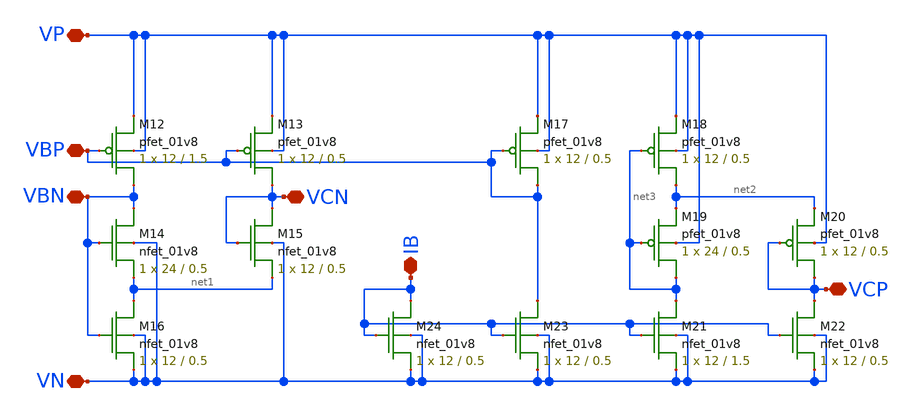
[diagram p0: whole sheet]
** sch_path: mp3/schematics/bias_generator.sch
**.subckt bias_generator VP VN IB VBP VCN VCP VBN
*.iopin VP
*.iopin VN
*.iopin IB
*.iopin VBP
*.iopin VCN
*.iopin VCP
*.iopin VBN
XM12 VBN VBP VP VP sky130_fd_pr__pfet_01v8 L=1.5 W=12 nf=1 ad='int((nf+1)/2) * W/nf * 0.29' as='int((nf+2)/2) * W/nf * 0.29'
+ pd='2*int((nf+1)/2) * (W/nf + 0.29)' ps='2*int((nf+2)/2) * (W/nf + 0.29)' nrd='0.29 / W' nrs='0.29 / W'
+ sa=0 sb=0 sd=0 mult=1 m=1
XM13 VCN VBP VP VP sky130_fd_pr__pfet_01v8 L=0.5 W=12 nf=1 ad='int((nf+1)/2) * W/nf * 0.29' as='int((nf+2)/2) * W/nf * 0.29'
+ pd='2*int((nf+1)/2) * (W/nf + 0.29)' ps='2*int((nf+2)/2) * (W/nf + 0.29)' nrd='0.29 / W' nrs='0.29 / W'
+ sa=0 sb=0 sd=0 mult=1 m=1
XM19 net3 net3 net2 VP sky130_fd_pr__pfet_01v8 L=0.5 W=24 nf=1 ad='int((nf+1)/2) * W/nf * 0.29' as='int((nf+2)/2) * W/nf * 0.29'
+ pd='2*int((nf+1)/2) * (W/nf + 0.29)' ps='2*int((nf+2)/2) * (W/nf + 0.29)' nrd='0.29 / W' nrs='0.29 / W'
+ sa=0 sb=0 sd=0 mult=1 m=1
XM20 VCP VCP net2 VP sky130_fd_pr__pfet_01v8 L=0.5 W=12 nf=1 ad='int((nf+1)/2) * W/nf * 0.29' as='int((nf+2)/2) * W/nf * 0.29'
+ pd='2*int((nf+1)/2) * (W/nf + 0.29)' ps='2*int((nf+2)/2) * (W/nf + 0.29)' nrd='0.29 / W' nrs='0.29 / W'
+ sa=0 sb=0 sd=0 mult=1 m=1
XM18 net2 net3 VP VP sky130_fd_pr__pfet_01v8 L=0.5 W=12 nf=1 ad='int((nf+1)/2) * W/nf * 0.29' as='int((nf+2)/2) * W/nf * 0.29'
+ pd='2*int((nf+1)/2) * (W/nf + 0.29)' ps='2*int((nf+2)/2) * (W/nf + 0.29)' nrd='0.29 / W' nrs='0.29 / W'
+ sa=0 sb=0 sd=0 mult=1 m=1
XM22 VCP IB VN VN sky130_fd_pr__nfet_01v8 L=0.5 W=12 nf=1 ad='int((nf+1)/2) * W/nf * 0.29' as='int((nf+2)/2) * W/nf * 0.29'
+ pd='2*int((nf+1)/2) * (W/nf + 0.29)' ps='2*int((nf+2)/2) * (W/nf + 0.29)' nrd='0.29 / W' nrs='0.29 / W'
+ sa=0 sb=0 sd=0 mult=1 m=1
XM21 net3 IB VN VN sky130_fd_pr__nfet_01v8 L=1.5 W=12 nf=1 ad='int((nf+1)/2) * W/nf * 0.29' as='int((nf+2)/2) * W/nf * 0.29'
+ pd='2*int((nf+1)/2) * (W/nf + 0.29)' ps='2*int((nf+2)/2) * (W/nf + 0.29)' nrd='0.29 / W' nrs='0.29 / W'
+ sa=0 sb=0 sd=0 mult=1 m=1
XM23 VBP IB VN VN sky130_fd_pr__nfet_01v8 L=0.5 W=12 nf=1 ad='int((nf+1)/2) * W/nf * 0.29' as='int((nf+2)/2) * W/nf * 0.29'
+ pd='2*int((nf+1)/2) * (W/nf + 0.29)' ps='2*int((nf+2)/2) * (W/nf + 0.29)' nrd='0.29 / W' nrs='0.29 / W'
+ sa=0 sb=0 sd=0 mult=1 m=1
XM24 IB IB VN VN sky130_fd_pr__nfet_01v8 L=0.5 W=12 nf=1 ad='int((nf+1)/2) * W/nf * 0.29' as='int((nf+2)/2) * W/nf * 0.29'
+ pd='2*int((nf+1)/2) * (W/nf + 0.29)' ps='2*int((nf+2)/2) * (W/nf + 0.29)' nrd='0.29 / W' nrs='0.29 / W'
+ sa=0 sb=0 sd=0 mult=1 m=1
XM15 VCN VCN net1 VN sky130_fd_pr__nfet_01v8 L=0.5 W=12 nf=1 ad='int((nf+1)/2) * W/nf * 0.29' as='int((nf+2)/2) * W/nf * 0.29'
+ pd='2*int((nf+1)/2) * (W/nf + 0.29)' ps='2*int((nf+2)/2) * (W/nf + 0.29)' nrd='0.29 / W' nrs='0.29 / W'
+ sa=0 sb=0 sd=0 mult=1 m=1
XM14 VBN VBN net1 VN sky130_fd_pr__nfet_01v8 L=0.5 W=24 nf=1 ad='int((nf+1)/2) * W/nf * 0.29' as='int((nf+2)/2) * W/nf * 0.29'
+ pd='2*int((nf+1)/2) * (W/nf + 0.29)' ps='2*int((nf+2)/2) * (W/nf + 0.29)' nrd='0.29 / W' nrs='0.29 / W'
+ sa=0 sb=0 sd=0 mult=1 m=1
XM16 net1 VBN VN VN sky130_fd_pr__nfet_01v8 L=0.5 W=12 nf=1 ad='int((nf+1)/2) * W/nf * 0.29' as='int((nf+2)/2) * W/nf * 0.29'
+ pd='2*int((nf+1)/2) * (W/nf + 0.29)' ps='2*int((nf+2)/2) * (W/nf + 0.29)' nrd='0.29 / W' nrs='0.29 / W'
+ sa=0 sb=0 sd=0 mult=1 m=1
XM17 VBP VBP VP VP sky130_fd_pr__pfet_01v8 L=0.5 W=12 nf=1 ad='int((nf+1)/2) * W/nf * 0.29' as='int((nf+2)/2) * W/nf * 0.29'
+ pd='2*int((nf+1)/2) * (W/nf + 0.29)' ps='2*int((nf+2)/2) * (W/nf + 0.29)' nrd='0.29 / W' nrs='0.29 / W'
+ sa=0 sb=0 sd=0 mult=1 m=1
**.ends
.end
